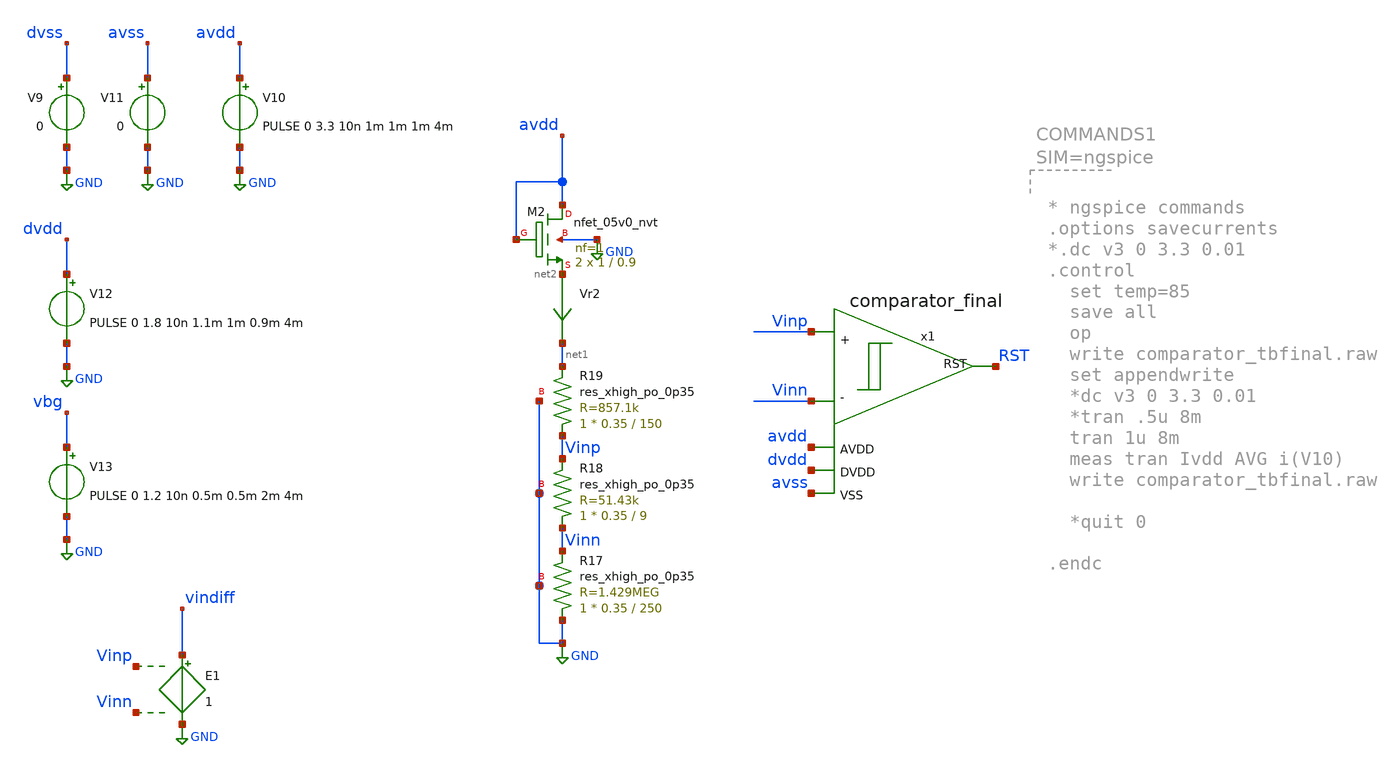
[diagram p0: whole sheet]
** sch_path: xschem_sim/comparator_tbfinal.sch
**.subckt comparator_tbfinal
x1 Vinn Vinp RST avss avdd dvdd comparator_final
V9 dvss GND 0
V10 avdd GND PULSE 0 3.3 10n 1m 1m 1m 4m
V11 avss GND 0
V12 dvdd GND PULSE 0 1.8 10n 1.1m 1m 0.9m 4m
V13 vbg GND PULSE 0 1.2 10n 0.5m 0.5m 2m 4m
Vr2 net2 net1 0
.save i(vr2)
XR17 GND Vinn GND sky130_fd_pr__res_xhigh_po_0p35 L=250 mult=1 m=1
XR18 Vinn Vinp GND sky130_fd_pr__res_xhigh_po_0p35 L=9 mult=1 m=1
XR19 Vinp net1 GND sky130_fd_pr__res_xhigh_po_0p35 L=150 mult=1 m=1
XM2 avdd avdd net2 GND sky130_fd_pr__nfet_05v0_nvt L=0.9 W=1 nf=1 ad='int((nf+1)/2) * W/nf * 0.29' as='int((nf+2)/2) * W/nf * 0.29'
+ pd='2*int((nf+1)/2) * (W/nf + 0.29)' ps='2*int((nf+2)/2) * (W/nf + 0.29)' nrd='0.29 / W' nrs='0.29 / W'
+ sa=0 sb=0 sd=0 mult=2 m=2
E1 vindiff GND Vinp Vinn 1
**** begin user architecture code
 .lib $::SKYWATER_MODELS/sky130.lib.spice tt

.include $::SKYWATER_STDCELLS/sky130_fd_sc_hd.spice
.include $::SKYWATER_STDCELLS/../../sky130_fd_sc_hvl/spice/sky130_fd_sc_hvl.spice





* ngspice commands
.options savecurrents
*.dc v3 0 3.3 0.01
.control
  set temp=85
  save all
  op
  write comparator_tbfinal.raw
  set appendwrite
  *dc v3 0 3.3 0.01
  *tran .5u 8m
  tran 1u 8m
  meas tran yAvdd1 FIND v(avdd) When v(RST)=0.9 RISE=1
  meas tran yAvdd2 FIND v(avdd) WHEN V(RST)=0.9 FALL=1
  meas tran Ivdd AVG i(V10)
  let hyst='yAvdd1-yAvdd2'
  print hyst
  write comparator_tbfinal.raw

  *quit 0

.endc



**** end user architecture code
**.ends
.GLOBAL GND
.end
